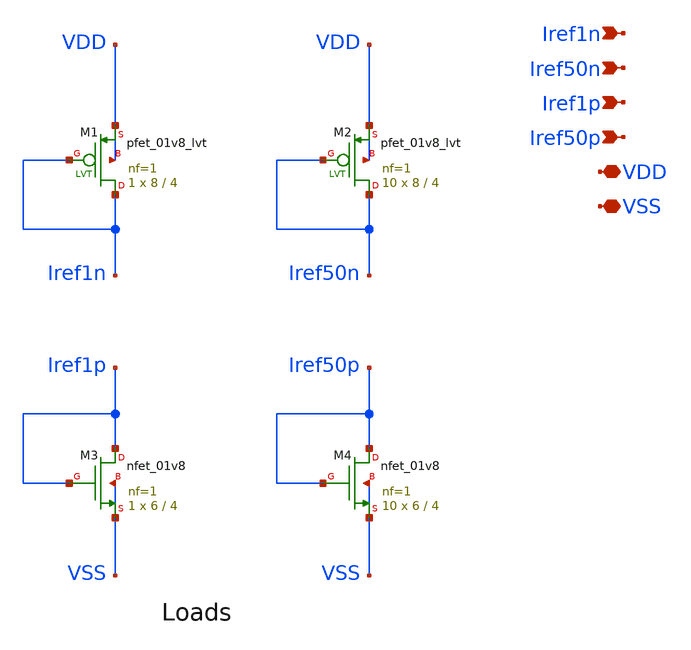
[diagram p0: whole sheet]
** sch_path: designs/used_and_to_delete/current_reference_load/xschem/current_reference_load.sch
**.subckt current_reference_load Iref1n VDD VSS Iref50n Iref1p Iref50p
*.ipin Iref1n
*.iopin VDD
*.iopin VSS
*.ipin Iref50n
*.ipin Iref1p
*.ipin Iref50p
XM3 Iref1p Iref1p VSS VSS sky130_fd_pr__nfet_01v8 L=4 W=6 nf=1 ad='int((nf+1)/2) * W/nf * 0.29' as='int((nf+2)/2) * W/nf * 0.29'
+ pd='2*int((nf+1)/2) * (W/nf + 0.29)' ps='2*int((nf+2)/2) * (W/nf + 0.29)' nrd='0.29 / W' nrs='0.29 / W'
+ sa=0 sb=0 sd=0 mult=1 m=1
XM1 Iref1n Iref1n VDD VDD sky130_fd_pr__pfet_01v8_lvt L=4 W=8 nf=1 ad='int((1 + 1)/2) * 8 / 1 * 0.29'
+ as='int((1 + 2)/2) * 8 / 1 * 0.29' pd='2*int((1 + 1)/2) * (8 / 1 + 0.29)' ps='2*int((1 + 2)/2) * (8 / 1 + 0.29)'
+ nrd='0.29 / 8 ' nrs='0.29 / 8 ' sa=0 sb=0 sd=0 mult=1 m=1
XM2 Iref50n Iref50n VDD VDD sky130_fd_pr__pfet_01v8_lvt L=4 W=8 nf=1 ad='int((1 + 1)/2) * 8 / 1 * 0.29'
+ as='int((1 + 2)/2) * 8 / 1 * 0.29' pd='2*int((1 + 1)/2) * (8 / 1 + 0.29)' ps='2*int((1 + 2)/2) * (8 / 1 + 0.29)'
+ nrd='0.29 / 8 ' nrs='0.29 / 8 ' sa=0 sb=0 sd=0 mult=10 m=10
XM4 Iref50p Iref50p VSS VSS sky130_fd_pr__nfet_01v8 L=4 W=6 nf=1 ad='int((nf+1)/2) * W/nf * 0.29' as='int((nf+2)/2) * W/nf * 0.29'
+ pd='2*int((nf+1)/2) * (W/nf + 0.29)' ps='2*int((nf+2)/2) * (W/nf + 0.29)' nrd='0.29 / W' nrs='0.29 / W'
+ sa=0 sb=0 sd=0 mult=10 m=10
**.ends
.end
